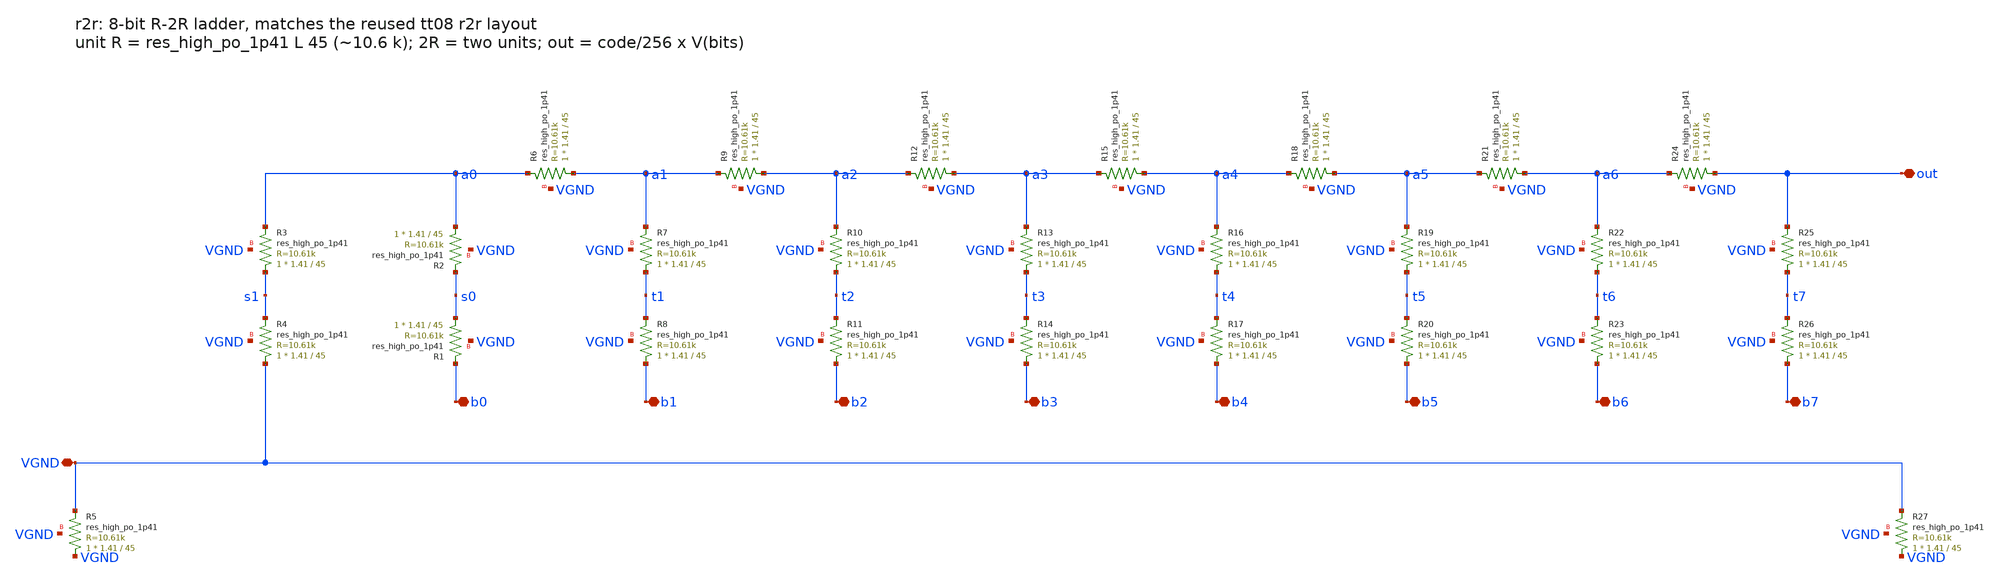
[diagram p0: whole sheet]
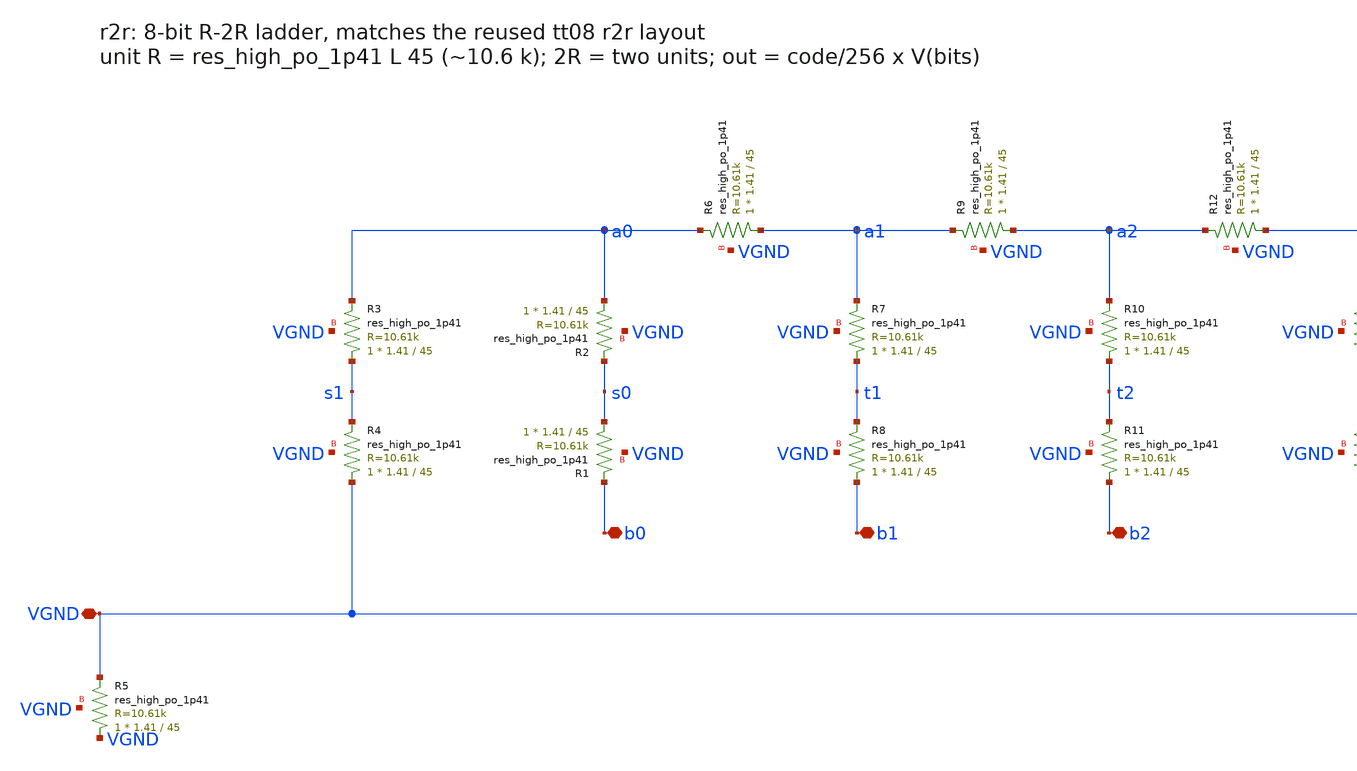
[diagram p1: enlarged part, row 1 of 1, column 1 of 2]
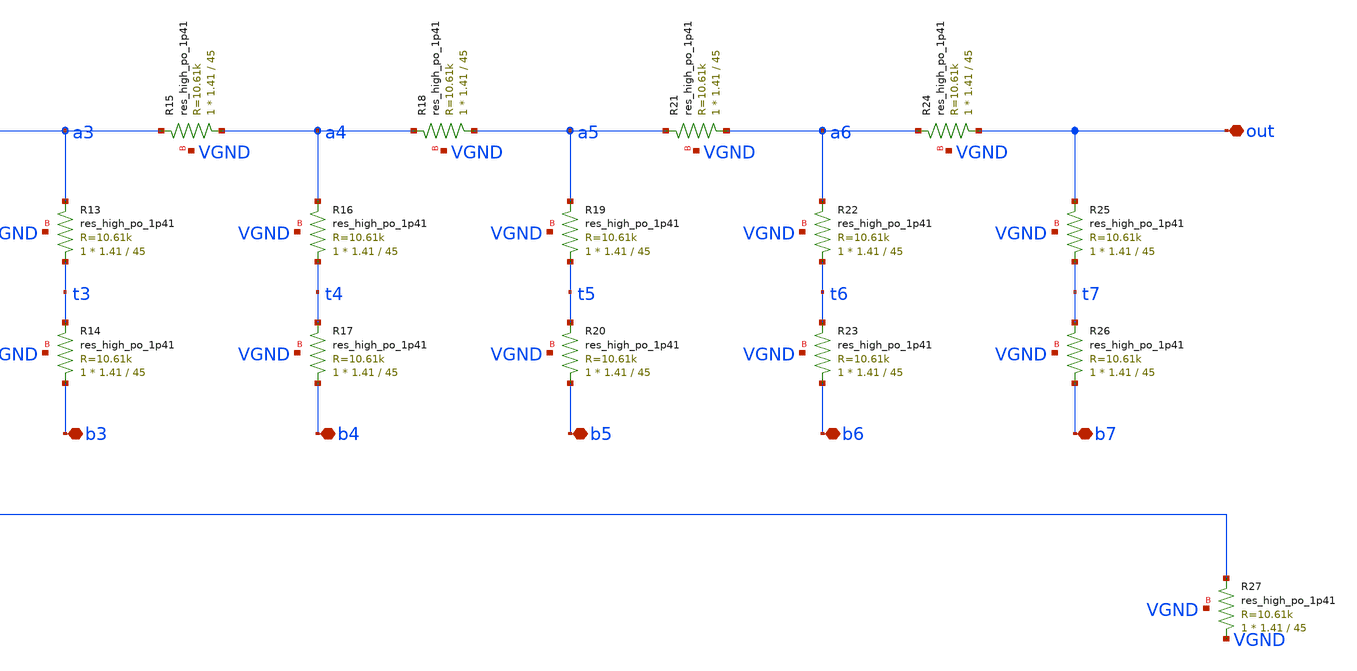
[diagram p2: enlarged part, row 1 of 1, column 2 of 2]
** sch_path: xschem/r2r.sch
**.subckt r2r b0 b1 b2 b3 b4 b5 b6 b7 out VGND
*.iopin b0
*.iopin b1
*.iopin b2
*.iopin b3
*.iopin b4
*.iopin b5
*.iopin b6
*.iopin b7
*.iopin out
*.iopin VGND
XR1 s0 b0 VGND sky130_fd_pr__res_high_po_1p41 L=45 mult=1 m=1
XR2 a0 s0 VGND sky130_fd_pr__res_high_po_1p41 L=45 mult=1 m=1
XR3 s1 a0 VGND sky130_fd_pr__res_high_po_1p41 L=45 mult=1 m=1
XR4 VGND s1 VGND sky130_fd_pr__res_high_po_1p41 L=45 mult=1 m=1
XR5 VGND VGND VGND sky130_fd_pr__res_high_po_1p41 L=45 mult=1 m=1
XR6 a1 a0 VGND sky130_fd_pr__res_high_po_1p41 L=45 mult=1 m=1
XR7 t1 a1 VGND sky130_fd_pr__res_high_po_1p41 L=45 mult=1 m=1
XR8 b1 t1 VGND sky130_fd_pr__res_high_po_1p41 L=45 mult=1 m=1
XR9 a2 a1 VGND sky130_fd_pr__res_high_po_1p41 L=45 mult=1 m=1
XR10 t2 a2 VGND sky130_fd_pr__res_high_po_1p41 L=45 mult=1 m=1
XR11 b2 t2 VGND sky130_fd_pr__res_high_po_1p41 L=45 mult=1 m=1
XR12 a3 a2 VGND sky130_fd_pr__res_high_po_1p41 L=45 mult=1 m=1
XR13 t3 a3 VGND sky130_fd_pr__res_high_po_1p41 L=45 mult=1 m=1
XR14 b3 t3 VGND sky130_fd_pr__res_high_po_1p41 L=45 mult=1 m=1
XR15 a4 a3 VGND sky130_fd_pr__res_high_po_1p41 L=45 mult=1 m=1
XR16 t4 a4 VGND sky130_fd_pr__res_high_po_1p41 L=45 mult=1 m=1
XR17 b4 t4 VGND sky130_fd_pr__res_high_po_1p41 L=45 mult=1 m=1
XR18 a5 a4 VGND sky130_fd_pr__res_high_po_1p41 L=45 mult=1 m=1
XR19 t5 a5 VGND sky130_fd_pr__res_high_po_1p41 L=45 mult=1 m=1
XR20 b5 t5 VGND sky130_fd_pr__res_high_po_1p41 L=45 mult=1 m=1
XR21 a6 a5 VGND sky130_fd_pr__res_high_po_1p41 L=45 mult=1 m=1
XR22 t6 a6 VGND sky130_fd_pr__res_high_po_1p41 L=45 mult=1 m=1
XR23 b6 t6 VGND sky130_fd_pr__res_high_po_1p41 L=45 mult=1 m=1
XR24 out a6 VGND sky130_fd_pr__res_high_po_1p41 L=45 mult=1 m=1
XR25 t7 out VGND sky130_fd_pr__res_high_po_1p41 L=45 mult=1 m=1
XR26 b7 t7 VGND sky130_fd_pr__res_high_po_1p41 L=45 mult=1 m=1
XR27 VGND VGND VGND sky130_fd_pr__res_high_po_1p41 L=45 mult=1 m=1
**.ends
.end
